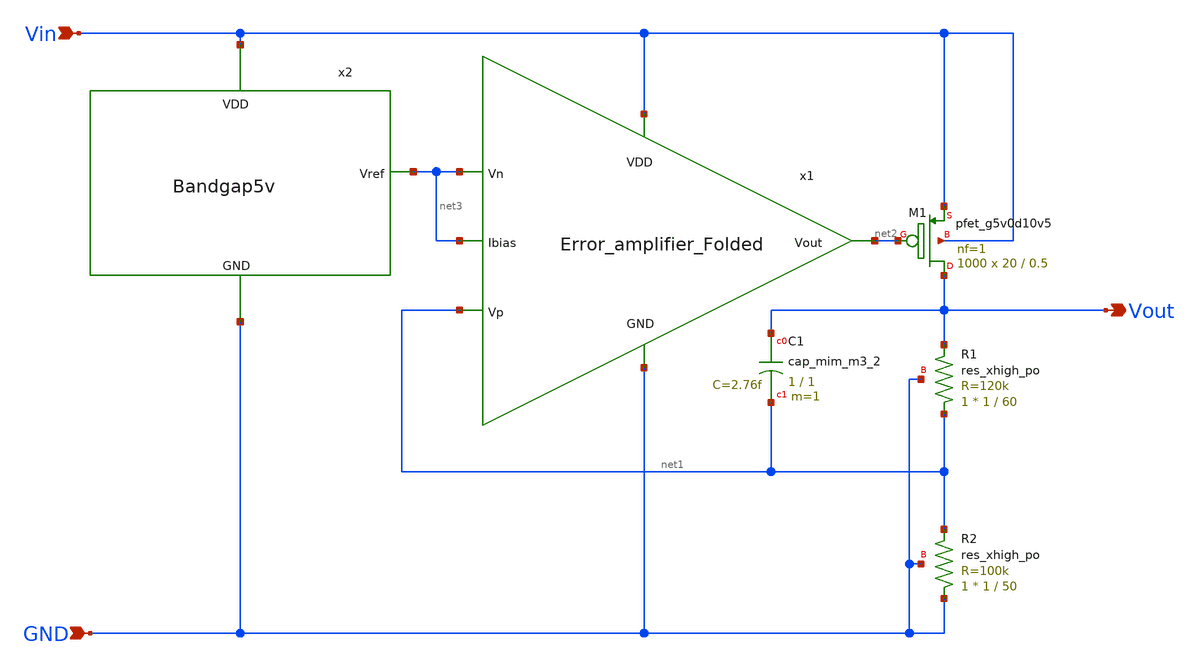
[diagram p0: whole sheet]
** sch_path: Analog_blocks/Analog_Blocks/LDO/Schematic/LDO_Folded_2.2v/LDO_Folded_2.2v.sch
**.subckt LDO_Folded_2.2v Vin GND Vout
*.ipin Vin
*.ipin GND
*.opin Vout
XR1 net1 Vout GND sky130_fd_pr__res_xhigh_po W=1 L=60 mult=1 m=1
XR2 GND net1 GND sky130_fd_pr__res_xhigh_po W=1 L=50 mult=1 m=1
XC1 Vout net1 sky130_fd_pr__cap_mim_m3_2 W=1 L=1 MF=1 m=1
XM1 Vout net2 Vin Vin sky130_fd_pr__pfet_g5v0d10v5 L=0.5 W=20 nf=1 ad='int((nf+1)/2) * W/nf * 0.29' as='int((nf+2)/2) * W/nf * 0.29'
+ pd='2*int((nf+1)/2) * (W/nf + 0.29)' ps='2*int((nf+2)/2) * (W/nf + 0.29)' nrd='0.29 / W' nrs='0.29 / W'
+ sa=0 sb=0 sd=0 mult=1000 m=1000
x1 Vin net2 net1 net3 net3 GND Error_amplifier_Folded
x2 net3 Vin GND Bandgap5v
**.ends

* expanding   symbol:
*+  /home/eslam/Analog_blocks/Analog_Blocks/LDO/Schematic/LDO_Folded_2.2v/Error_amplifier_Folded.sym # of pins=6
** sym_path: Analog_Blocks/LDO/Schematic/LDO_Folded_1.8v/Error_amplifier_Folded.sym
** sch_path: Analog_Blocks/LDO/Schematic/LDO_Folded_1.8v/Error_amplifier_Folded.sch
.subckt Error_amplifier_Folded VDD Vout Vp Vn Ibias GND
*.ipin VDD
*.ipin GND
*.ipin Vp
*.ipin Vn
*.opin Vout
*.ipin Ibias
XM1 net3 Vp net1 GND sky130_fd_pr__nfet_g5v0d10v5 L=0.5 W=50 nf=1 ad='int((nf+1)/2) * W/nf * 0.29' as='int((nf+2)/2) * W/nf * 0.29'
+ pd='2*int((nf+1)/2) * (W/nf + 0.29)' ps='2*int((nf+2)/2) * (W/nf + 0.29)' nrd='0.29 / W' nrs='0.29 / W'
+ sa=0 sb=0 sd=0 mult=1 m=1
XM2 net2 Vn net1 GND sky130_fd_pr__nfet_g5v0d10v5 L=0.5 W=50 nf=1 ad='int((nf+1)/2) * W/nf * 0.29' as='int((nf+2)/2) * W/nf * 0.29'
+ pd='2*int((nf+1)/2) * (W/nf + 0.29)' ps='2*int((nf+2)/2) * (W/nf + 0.29)' nrd='0.29 / W' nrs='0.29 / W'
+ sa=0 sb=0 sd=0 mult=1 m=1
XM9 Vout net4 GND GND sky130_fd_pr__nfet_g5v0d10v5 L=2 W=6 nf=1 ad='int((nf+1)/2) * W/nf * 0.29' as='int((nf+2)/2) * W/nf * 0.29'
+ pd='2*int((nf+1)/2) * (W/nf + 0.29)' ps='2*int((nf+2)/2) * (W/nf + 0.29)' nrd='0.29 / W' nrs='0.29 / W'
+ sa=0 sb=0 sd=0 mult=1 m=1
XM6 net4 net6 net3 VDD sky130_fd_pr__pfet_g5v0d10v5 L=0.5 W=40 nf=1 ad='int((nf+1)/2) * W/nf * 0.29'
+ as='int((nf+2)/2) * W/nf * 0.29' pd='2*int((nf+1)/2) * (W/nf + 0.29)' ps='2*int((nf+2)/2) * (W/nf + 0.29)'
+ nrd='0.29 / W' nrs='0.29 / W' sa=0 sb=0 sd=0 mult=1 m=1
XM5 net2 net5 VDD VDD sky130_fd_pr__pfet_g5v0d10v5 L=0.5 W=40 nf=1 ad='int((nf+1)/2) * W/nf * 0.29' as='int((nf+2)/2) * W/nf * 0.29'
+ pd='2*int((nf+1)/2) * (W/nf + 0.29)' ps='2*int((nf+2)/2) * (W/nf + 0.29)' nrd='0.29 / W' nrs='0.29 / W'
+ sa=0 sb=0 sd=0 mult=1 m=1
XM4 net3 net5 VDD VDD sky130_fd_pr__pfet_g5v0d10v5 L=0.5 W=40 nf=1 ad='int((nf+1)/2) * W/nf * 0.29' as='int((nf+2)/2) * W/nf * 0.29'
+ pd='2*int((nf+1)/2) * (W/nf + 0.29)' ps='2*int((nf+2)/2) * (W/nf + 0.29)' nrd='0.29 / W' nrs='0.29 / W'
+ sa=0 sb=0 sd=0 mult=1 m=1
XM3 net1 Ibias GND GND sky130_fd_pr__nfet_g5v0d10v5 L=0.9 W=12 nf=1 ad='int((nf+1)/2) * W/nf * 0.29'
+ as='int((nf+2)/2) * W/nf * 0.29' pd='2*int((nf+1)/2) * (W/nf + 0.29)' ps='2*int((nf+2)/2) * (W/nf + 0.29)'
+ nrd='0.29 / W' nrs='0.29 / W' sa=0 sb=0 sd=0 mult=1 m=1
XM7 Vout net6 net2 VDD sky130_fd_pr__pfet_g5v0d10v5 L=0.5 W=40 nf=1 ad='int((nf+1)/2) * W/nf * 0.29'
+ as='int((nf+2)/2) * W/nf * 0.29' pd='2*int((nf+1)/2) * (W/nf + 0.29)' ps='2*int((nf+2)/2) * (W/nf + 0.29)'
+ nrd='0.29 / W' nrs='0.29 / W' sa=0 sb=0 sd=0 mult=1 m=1
XM8 net4 net4 GND GND sky130_fd_pr__nfet_g5v0d10v5 L=2 W=6 nf=1 ad='int((nf+1)/2) * W/nf * 0.29' as='int((nf+2)/2) * W/nf * 0.29'
+ pd='2*int((nf+1)/2) * (W/nf + 0.29)' ps='2*int((nf+2)/2) * (W/nf + 0.29)' nrd='0.29 / W' nrs='0.29 / W'
+ sa=0 sb=0 sd=0 mult=1 m=1
XM10 Ibias Ibias GND GND sky130_fd_pr__nfet_g5v0d10v5 L=0.9 W=12 nf=1 ad='int((nf+1)/2) * W/nf * 0.29'
+ as='int((nf+2)/2) * W/nf * 0.29' pd='2*int((nf+1)/2) * (W/nf + 0.29)' ps='2*int((nf+2)/2) * (W/nf + 0.29)'
+ nrd='0.29 / W' nrs='0.29 / W' sa=0 sb=0 sd=0 mult=1 m=1
XM11 net5 Ibias GND GND sky130_fd_pr__nfet_g5v0d10v5 L=0.9 W=6 nf=1 ad='int((nf+1)/2) * W/nf * 0.29'
+ as='int((nf+2)/2) * W/nf * 0.29' pd='2*int((nf+1)/2) * (W/nf + 0.29)' ps='2*int((nf+2)/2) * (W/nf + 0.29)'
+ nrd='0.29 / W' nrs='0.29 / W' sa=0 sb=0 sd=0 mult=1 m=1
XM12 net6 Ibias GND GND sky130_fd_pr__nfet_g5v0d10v5 L=0.9 W=6 nf=1 ad='int((nf+1)/2) * W/nf * 0.29'
+ as='int((nf+2)/2) * W/nf * 0.29' pd='2*int((nf+1)/2) * (W/nf + 0.29)' ps='2*int((nf+2)/2) * (W/nf + 0.29)'
+ nrd='0.29 / W' nrs='0.29 / W' sa=0 sb=0 sd=0 mult=1 m=1
XM13 net5 net5 VDD VDD sky130_fd_pr__pfet_g5v0d10v5 L=0.5 W=13.5 nf=1 ad='int((nf+1)/2) * W/nf * 0.29'
+ as='int((nf+2)/2) * W/nf * 0.29' pd='2*int((nf+1)/2) * (W/nf + 0.29)' ps='2*int((nf+2)/2) * (W/nf + 0.29)'
+ nrd='0.29 / W' nrs='0.29 / W' sa=0 sb=0 sd=0 mult=1 m=1
XM14 net6 net6 VDD VDD sky130_fd_pr__pfet_g5v0d10v5 L=1 W=2 nf=1 ad='int((nf+1)/2) * W/nf * 0.29' as='int((nf+2)/2) * W/nf * 0.29'
+ pd='2*int((nf+1)/2) * (W/nf + 0.29)' ps='2*int((nf+2)/2) * (W/nf + 0.29)' nrd='0.29 / W' nrs='0.29 / W'
+ sa=0 sb=0 sd=0 mult=1 m=1
.ends


* expanding   symbol:
*+  /home/eslam/Analog_blocks/Analog_Blocks/LDO/Schematic/LDO_Folded_2.2v/Bandgap5v.sym # of pins=3
** sym_path: Analog_Blocks/Bandgap/Schematics/BGR5v/Bandgap5v.sym
** sch_path: Analog_Blocks/Bandgap/Schematics/BGR5v/Bandgap5v.sch
.subckt Bandgap5v Vref VDD GND
*.ipin VDD
*.ipin GND
*.opin Vref
XQ1 GND GND net3 sky130_fd_pr__pnp_05v5_W0p68L0p68 m=1
XQ2 GND GND net1 sky130_fd_pr__pnp_05v5_W0p68L0p68 m=1
XQ3 GND GND net1 sky130_fd_pr__pnp_05v5_W0p68L0p68 m=1
XQ4 GND GND net1 sky130_fd_pr__pnp_05v5_W0p68L0p68 m=1
XQ5 GND GND net1 sky130_fd_pr__pnp_05v5_W0p68L0p68 m=1
XQ6 GND GND net1 sky130_fd_pr__pnp_05v5_W0p68L0p68 m=1
XQ7 GND GND net1 sky130_fd_pr__pnp_05v5_W0p68L0p68 m=1
XQ8 GND GND net1 sky130_fd_pr__pnp_05v5_W0p68L0p68 m=1
XQ9 GND GND net1 sky130_fd_pr__pnp_05v5_W0p68L0p68 m=1
XM2 net4 net5 VDD VDD sky130_fd_pr__pfet_g5v0d10v5 L=1 W=10 nf=1 ad='int((nf+1)/2) * W/nf * 0.29' as='int((nf+2)/2) * W/nf * 0.29'
+ pd='2*int((nf+1)/2) * (W/nf + 0.29)' ps='2*int((nf+2)/2) * (W/nf + 0.29)' nrd='0.29 / W' nrs='0.29 / W'
+ sa=0 sb=0 sd=0 mult=1 m=1
XM3 net3 net4 VDD VDD sky130_fd_pr__pfet_g5v0d10v5 L=1 W=10 nf=1 ad='int((nf+1)/2) * W/nf * 0.29' as='int((nf+2)/2) * W/nf * 0.29'
+ pd='2*int((nf+1)/2) * (W/nf + 0.29)' ps='2*int((nf+2)/2) * (W/nf + 0.29)' nrd='0.29 / W' nrs='0.29 / W'
+ sa=0 sb=0 sd=0 mult=1 m=1
XM1 net4 net5 GND GND sky130_fd_pr__nfet_g5v0d10v5 L=40 W=1 nf=1 ad='int((nf+1)/2) * W/nf * 0.29' as='int((nf+2)/2) * W/nf * 0.29'
+ pd='2*int((nf+1)/2) * (W/nf + 0.29)' ps='2*int((nf+2)/2) * (W/nf + 0.29)' nrd='0.29 / W' nrs='0.29 / W'
+ sa=0 sb=0 sd=0 mult=1 m=1
XR1 net2 Vref GND sky130_fd_pr__res_high_po W=1 L=6 mult=1 m=1
XR3 net3 Vref GND sky130_fd_pr__res_high_po W=1 L=6 mult=1 m=1
XR2 net1 net2 GND sky130_fd_pr__res_high_po W=1 L=2.6 mult=1 m=1
x1 VDD net3 net2 Vref net5 GND Bandgap5v_OTA
.ends


* expanding   symbol:  /home/eslam/Analog_Design/LDO/Schematic/Bandgap5v_OTA.sym # of pins=6
** sym_path: LDO/Schematic/Bandgap5v_OTA.sym
** sch_path: LDO/Schematic/Bandgap5v_OTA.sch
.subckt Bandgap5v_OTA Vdd Vn Vp Ibias Vhigh Gnd
*.opin Ibias
*.ipin Vhigh
*.ipin Vdd
*.ipin Gnd
*.ipin Vn
*.ipin Vp
XM6 Ibias Vhigh Vdd Vdd sky130_fd_pr__pfet_g5v0d10v5 L=1 W=10 nf=1 ad='int((nf+1)/2) * W/nf * 0.29' as='int((nf+2)/2) * W/nf * 0.29'
+ pd='2*int((nf+1)/2) * (W/nf + 0.29)' ps='2*int((nf+2)/2) * (W/nf + 0.29)' nrd='0.29 / W' nrs='0.29 / W'
+ sa=0 sb=0 sd=0 mult=1 m=1
XM5 net3 Vhigh Vdd Vdd sky130_fd_pr__pfet_g5v0d10v5 L=1 W=10 nf=1 ad='int((nf+1)/2) * W/nf * 0.29' as='int((nf+2)/2) * W/nf * 0.29'
+ pd='2*int((nf+1)/2) * (W/nf + 0.29)' ps='2*int((nf+2)/2) * (W/nf + 0.29)' nrd='0.29 / W' nrs='0.29 / W'
+ sa=0 sb=0 sd=0 mult=1 m=1
XM7 Vhigh Vhigh Vdd Vdd sky130_fd_pr__pfet_g5v0d10v5 L=1 W=54 nf=1 ad='int((nf+1)/2) * W/nf * 0.29' as='int((nf+2)/2) * W/nf * 0.29'
+ pd='2*int((nf+1)/2) * (W/nf + 0.29)' ps='2*int((nf+2)/2) * (W/nf + 0.29)' nrd='0.29 / W' nrs='0.29 / W'
+ sa=0 sb=0 sd=0 mult=1 m=1
XM2 net1 Vp net3 Vdd sky130_fd_pr__pfet_g5v0d10v5 L=1 W=30 nf=1 ad='int((nf+1)/2) * W/nf * 0.29' as='int((nf+2)/2) * W/nf * 0.29'
+ pd='2*int((nf+1)/2) * (W/nf + 0.29)' ps='2*int((nf+2)/2) * (W/nf + 0.29)' nrd='0.29 / W' nrs='0.29 / W'
+ sa=0 sb=0 sd=0 mult=1 m=1
XM1 net2 Vn net3 Vdd sky130_fd_pr__pfet_g5v0d10v5 L=1 W=30 nf=1 ad='int((nf+1)/2) * W/nf * 0.29' as='int((nf+2)/2) * W/nf * 0.29'
+ pd='2*int((nf+1)/2) * (W/nf + 0.29)' ps='2*int((nf+2)/2) * (W/nf + 0.29)' nrd='0.29 / W' nrs='0.29 / W'
+ sa=0 sb=0 sd=0 mult=1 m=1
XM8 Vhigh net1 Gnd Gnd sky130_fd_pr__nfet_g5v0d10v5 L=0.5 W=75 nf=1 ad='int((nf+1)/2) * W/nf * 0.29'
+ as='int((nf+2)/2) * W/nf * 0.29' pd='2*int((nf+1)/2) * (W/nf + 0.29)' ps='2*int((nf+2)/2) * (W/nf + 0.29)'
+ nrd='0.29 / W' nrs='0.29 / W' sa=0 sb=0 sd=0 mult=1 m=1
XM4 net1 net2 Gnd Gnd sky130_fd_pr__nfet_g5v0d10v5 L=0.5 W=7.5 nf=1 ad='int((nf+1)/2) * W/nf * 0.29'
+ as='int((nf+2)/2) * W/nf * 0.29' pd='2*int((nf+1)/2) * (W/nf + 0.29)' ps='2*int((nf+2)/2) * (W/nf + 0.29)'
+ nrd='0.29 / W' nrs='0.29 / W' sa=0 sb=0 sd=0 mult=1 m=1
XM3 net2 net2 Gnd Gnd sky130_fd_pr__nfet_g5v0d10v5 L=0.5 W=7.5 nf=1 ad='int((nf+1)/2) * W/nf * 0.29'
+ as='int((nf+2)/2) * W/nf * 0.29' pd='2*int((nf+1)/2) * (W/nf + 0.29)' ps='2*int((nf+2)/2) * (W/nf + 0.29)'
+ nrd='0.29 / W' nrs='0.29 / W' sa=0 sb=0 sd=0 mult=1 m=1
XC1 net1 Vhigh sky130_fd_pr__cap_mim_m3_2 W=1 L=1 MF=1 m=1
.ends

.end
